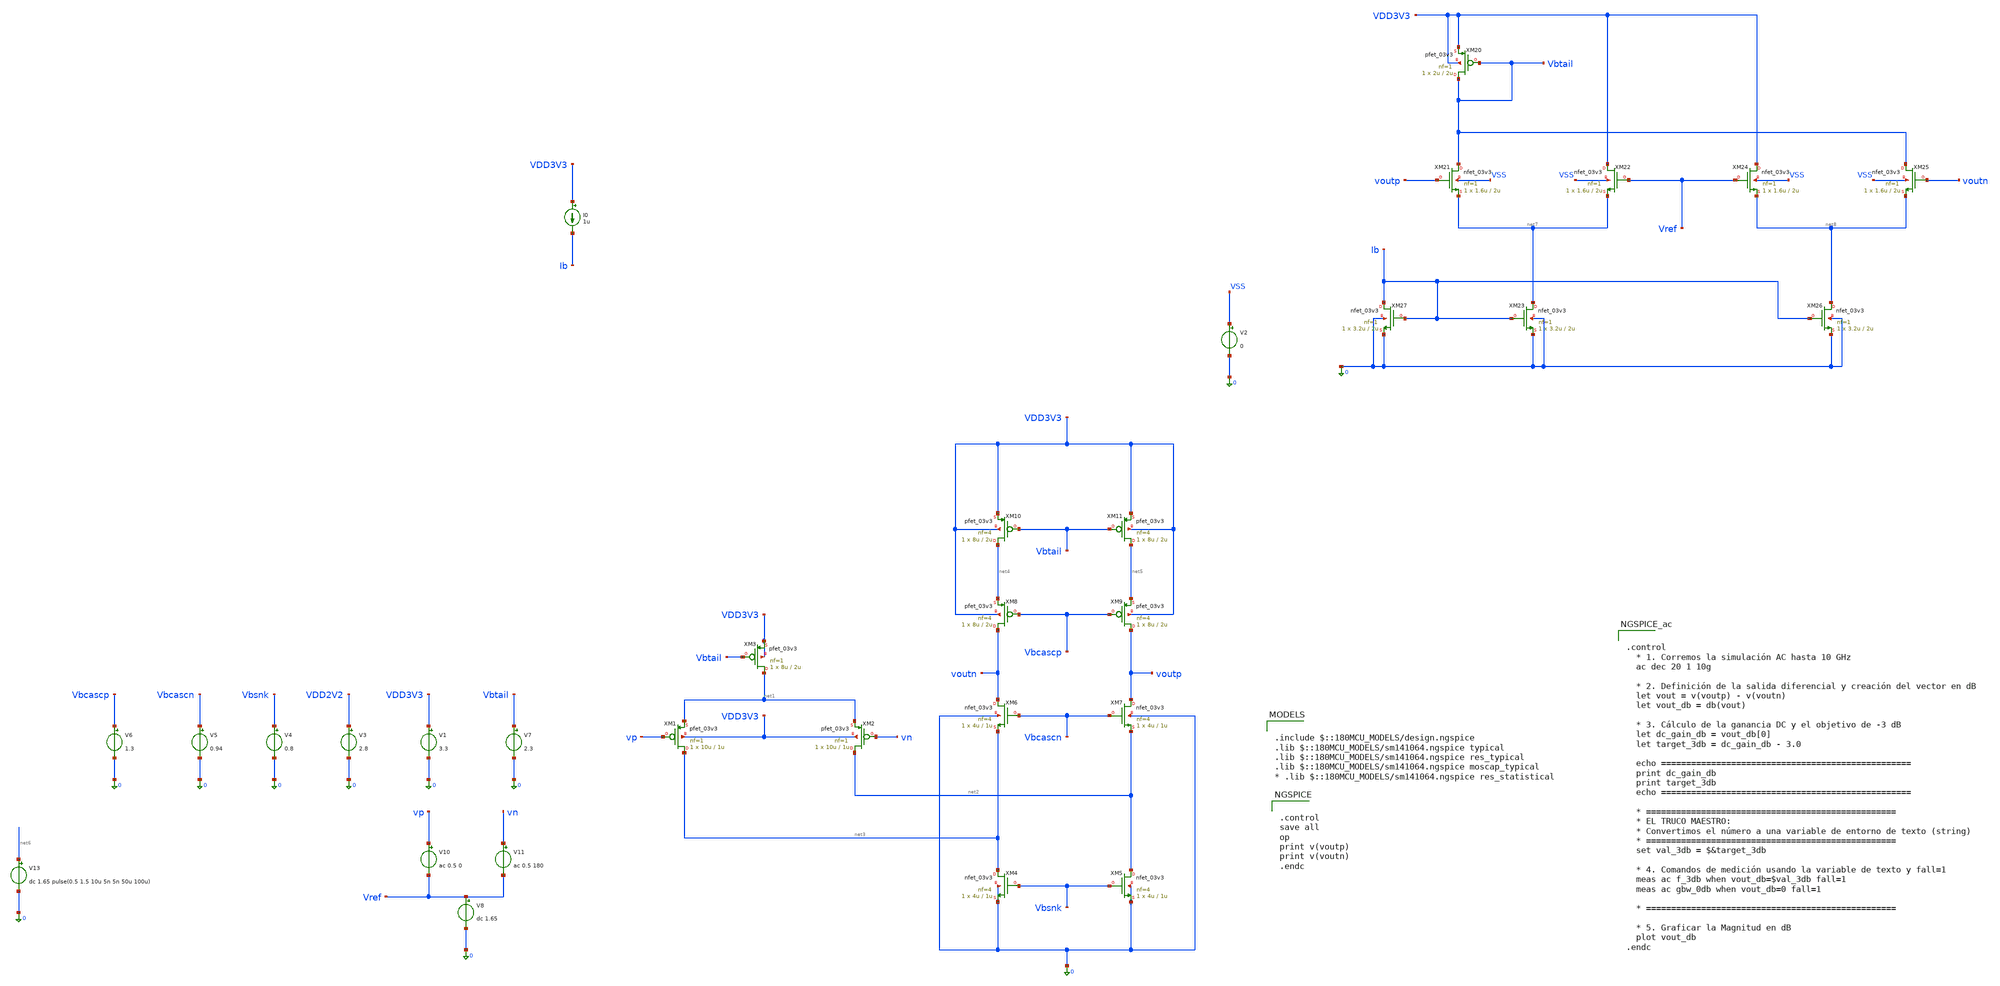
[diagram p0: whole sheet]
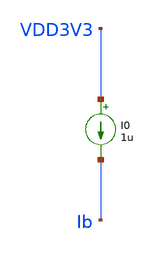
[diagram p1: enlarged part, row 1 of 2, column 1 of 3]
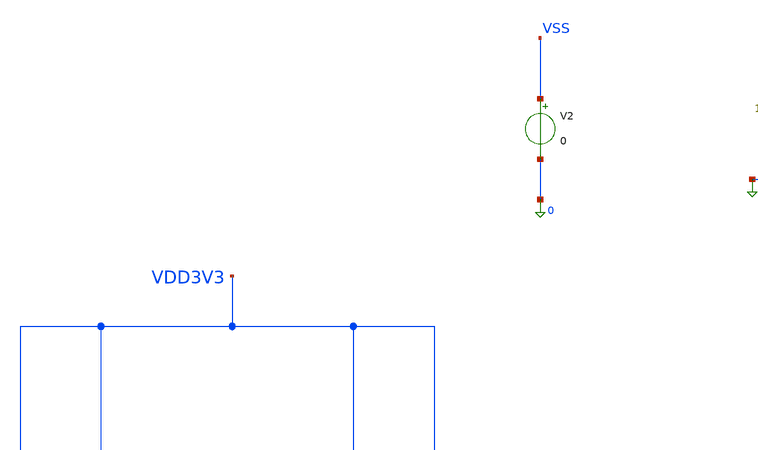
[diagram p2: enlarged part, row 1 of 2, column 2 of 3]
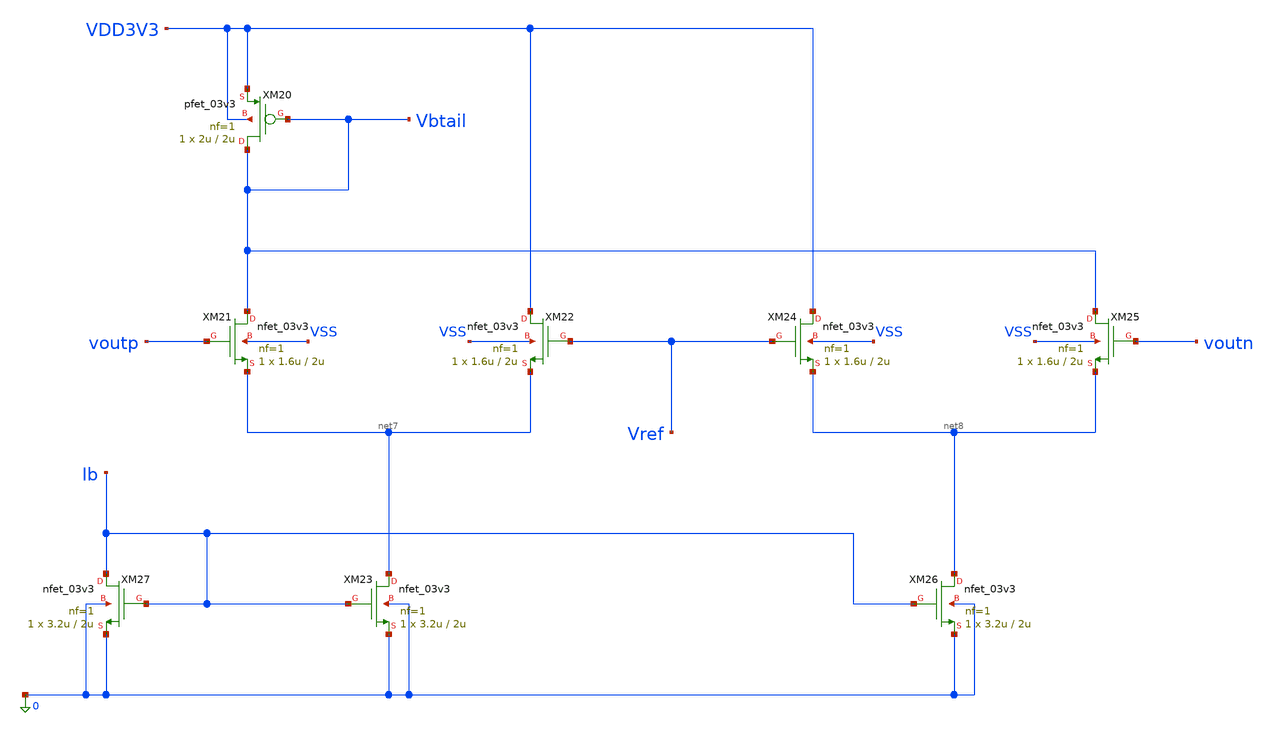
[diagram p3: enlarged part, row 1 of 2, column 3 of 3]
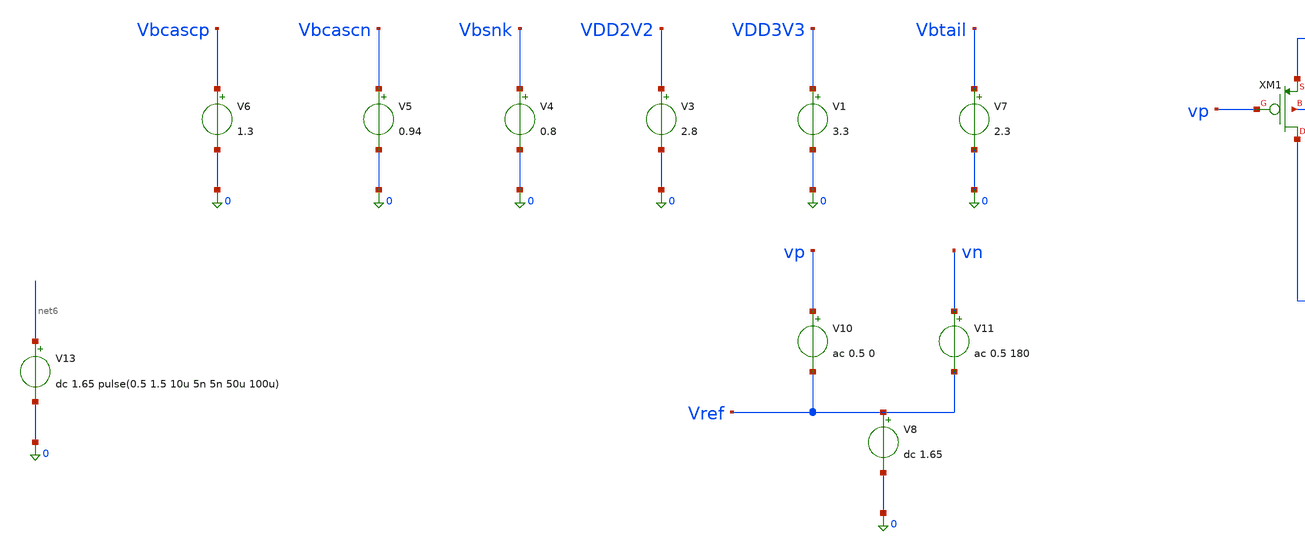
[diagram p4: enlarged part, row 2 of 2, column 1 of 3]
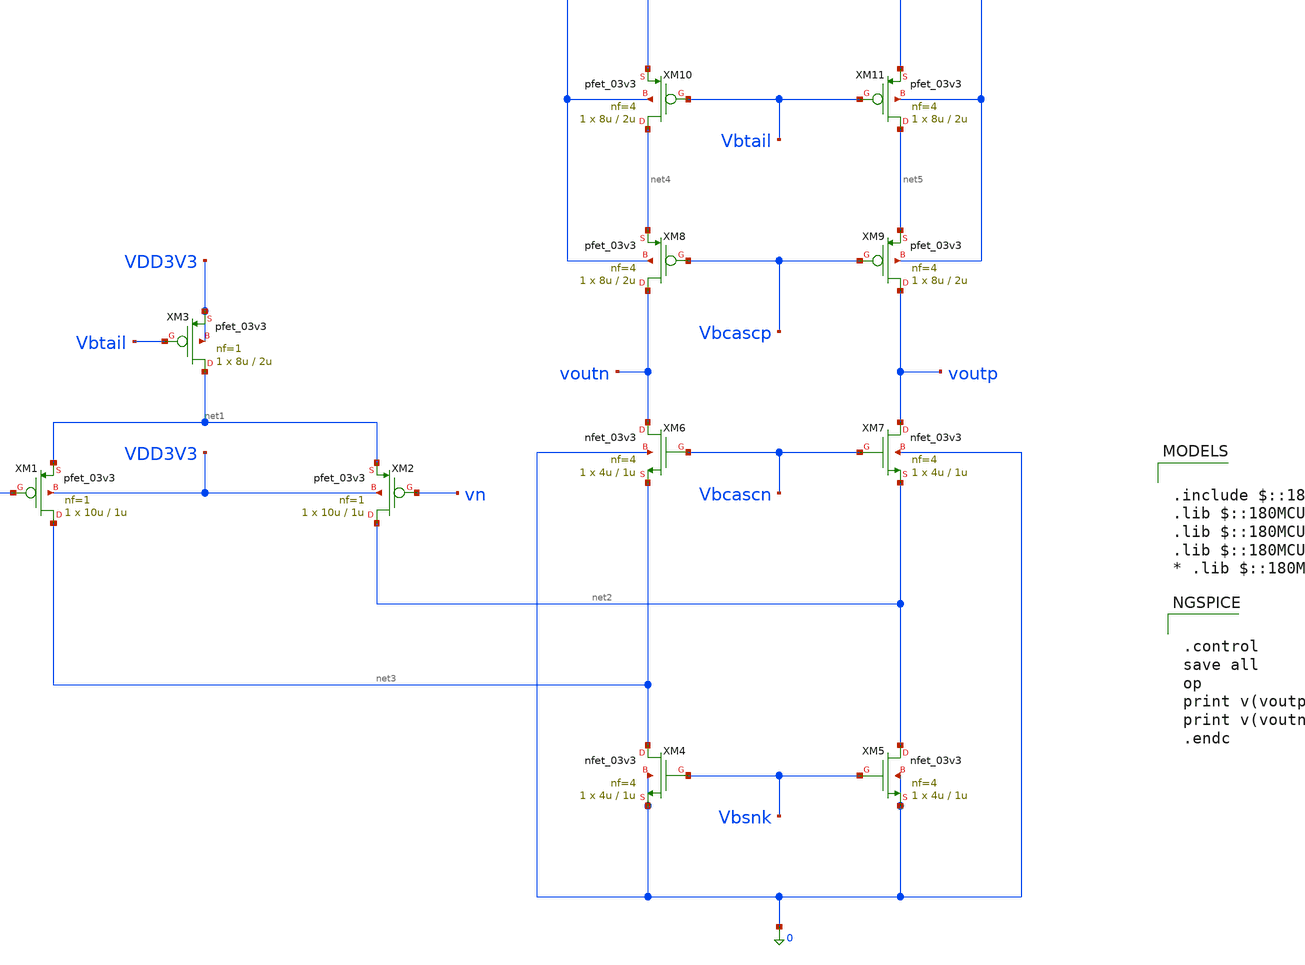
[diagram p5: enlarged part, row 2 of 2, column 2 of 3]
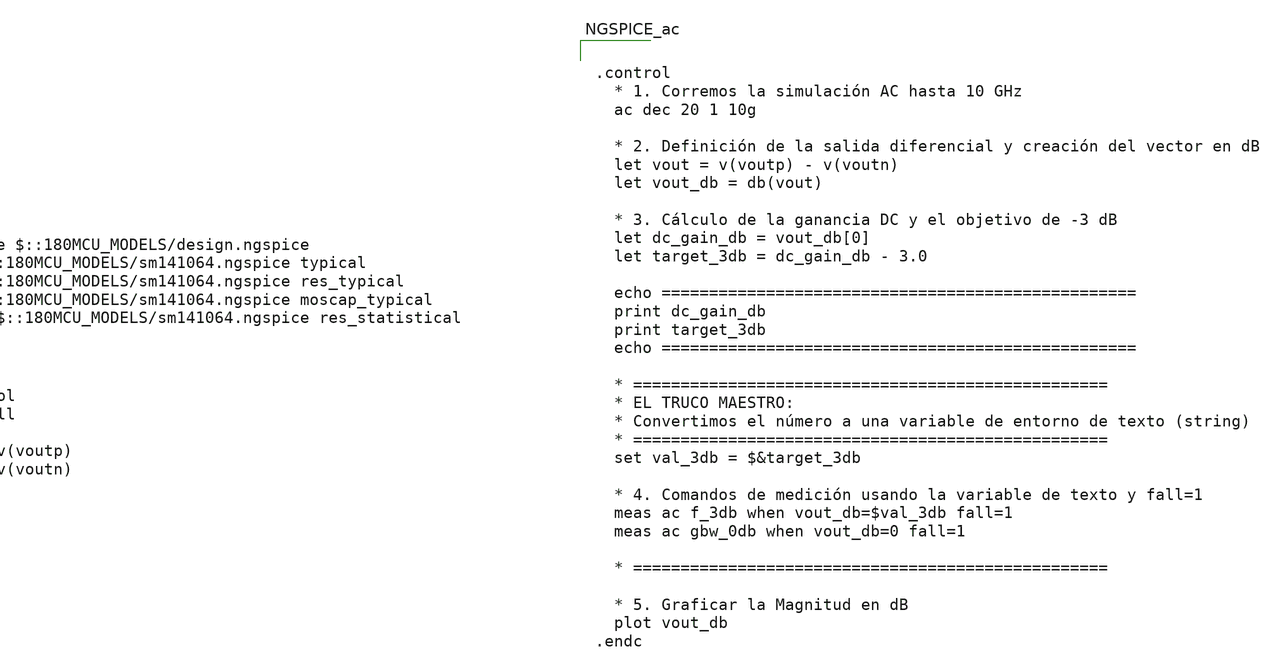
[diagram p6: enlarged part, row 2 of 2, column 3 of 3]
** sch_path: designs/libs/core_pga/folded_cascode/tb_folded_cascode_v2.sch
**.subckt tb_folded_cascode_v2
XM1 net3 vp net1 VDD3V3 pfet_03v3 L=1u W=10u nf=1 ad='int((nf+1)/2) * W/nf * 0.18u' as='int((nf+2)/2) * W/nf * 0.18u'
+ pd='2*int((nf+1)/2) * (W/nf + 0.18u)' ps='2*int((nf+2)/2) * (W/nf + 0.18u)' nrd='0.18u / W' nrs='0.18u / W'
+ sa=0 sb=0 sd=0 m=1
V1 VDD3V3 0 3.3
XM2 net2 vn net1 VDD3V3 pfet_03v3 L=1u W=10u nf=1 ad='int((nf+1)/2) * W/nf * 0.18u' as='int((nf+2)/2) * W/nf * 0.18u'
+ pd='2*int((nf+1)/2) * (W/nf + 0.18u)' ps='2*int((nf+2)/2) * (W/nf + 0.18u)' nrd='0.18u / W' nrs='0.18u / W'
+ sa=0 sb=0 sd=0 m=1
V3 VDD2V2 0 2.8
V4 Vbsnk 0 0.8
V5 Vbcascn 0 0.94
V6 Vbcascp 0 1.3
V8 Vref 0 dc 1.65
V10 vp Vref ac 0.5 0
V11 vn Vref ac 0.5 180
XM6 voutn Vbcascn net3 0 nfet_03v3 L=1u W=4u nf=4 ad='int((nf+1)/2) * W/nf * 0.18u' as='int((nf+2)/2) * W/nf * 0.18u'
+ pd='2*int((nf+1)/2) * (W/nf + 0.18u)' ps='2*int((nf+2)/2) * (W/nf + 0.18u)' nrd='0.18u / W' nrs='0.18u / W'
+ sa=0 sb=0 sd=0 m=1
XM7 voutp Vbcascn net2 0 nfet_03v3 L=1u W=4u nf=4 ad='int((nf+1)/2) * W/nf * 0.18u' as='int((nf+2)/2) * W/nf * 0.18u'
+ pd='2*int((nf+1)/2) * (W/nf + 0.18u)' ps='2*int((nf+2)/2) * (W/nf + 0.18u)' nrd='0.18u / W' nrs='0.18u / W'
+ sa=0 sb=0 sd=0 m=1
XM8 voutn Vbcascp net4 VDD3V3 pfet_03v3 L=2u W=8u nf=4 ad='int((nf+1)/2) * W/nf * 0.18u' as='int((nf+2)/2) * W/nf * 0.18u'
+ pd='2*int((nf+1)/2) * (W/nf + 0.18u)' ps='2*int((nf+2)/2) * (W/nf + 0.18u)' nrd='0.18u / W' nrs='0.18u / W'
+ sa=0 sb=0 sd=0 m=1
XM9 voutp Vbcascp net5 VDD3V3 pfet_03v3 L=2u W=8u nf=4 ad='int((nf+1)/2) * W/nf * 0.18u' as='int((nf+2)/2) * W/nf * 0.18u'
+ pd='2*int((nf+1)/2) * (W/nf + 0.18u)' ps='2*int((nf+2)/2) * (W/nf + 0.18u)' nrd='0.18u / W' nrs='0.18u / W'
+ sa=0 sb=0 sd=0 m=1
V7 Vbtail 0 2.3
XM3 net1 Vbtail VDD3V3 VDD3V3 pfet_03v3 L=2u W=8u nf=1 ad='int((nf+1)/2) * W/nf * 0.18u' as='int((nf+2)/2) * W/nf * 0.18u'
+ pd='2*int((nf+1)/2) * (W/nf + 0.18u)' ps='2*int((nf+2)/2) * (W/nf + 0.18u)' nrd='0.18u / W' nrs='0.18u / W'
+ sa=0 sb=0 sd=0 m=1
XM4 net3 Vbsnk 0 0 nfet_03v3 L=1u W=4u nf=4 ad='int((nf+1)/2) * W/nf * 0.18u' as='int((nf+2)/2) * W/nf * 0.18u'
+ pd='2*int((nf+1)/2) * (W/nf + 0.18u)' ps='2*int((nf+2)/2) * (W/nf + 0.18u)' nrd='0.18u / W' nrs='0.18u / W'
+ sa=0 sb=0 sd=0 m=1
XM5 net2 Vbsnk 0 0 nfet_03v3 L=1u W=4u nf=4 ad='int((nf+1)/2) * W/nf * 0.18u' as='int((nf+2)/2) * W/nf * 0.18u'
+ pd='2*int((nf+1)/2) * (W/nf + 0.18u)' ps='2*int((nf+2)/2) * (W/nf + 0.18u)' nrd='0.18u / W' nrs='0.18u / W'
+ sa=0 sb=0 sd=0 m=1
XM10 net4 Vbtail VDD3V3 VDD3V3 pfet_03v3 L=2u W=8u nf=4 ad='int((nf+1)/2) * W/nf * 0.18u' as='int((nf+2)/2) * W/nf * 0.18u'
+ pd='2*int((nf+1)/2) * (W/nf + 0.18u)' ps='2*int((nf+2)/2) * (W/nf + 0.18u)' nrd='0.18u / W' nrs='0.18u / W'
+ sa=0 sb=0 sd=0 m=1
XM11 net5 Vbtail VDD3V3 VDD3V3 pfet_03v3 L=2u W=8u nf=4 ad='int((nf+1)/2) * W/nf * 0.18u' as='int((nf+2)/2) * W/nf * 0.18u'
+ pd='2*int((nf+1)/2) * (W/nf + 0.18u)' ps='2*int((nf+2)/2) * (W/nf + 0.18u)' nrd='0.18u / W' nrs='0.18u / W'
+ sa=0 sb=0 sd=0 m=1
V13 net6 0 dc 1.65 pulse(0.5 1.5 10u 5n 5n 50u 100u)
I0 VDD3V3 Ib 1u
XM20 Vbtail Vbtail VDD3V3 VDD3V3 pfet_03v3 L=2u W=2u nf=1 ad='int((nf+1)/2) * W/nf * 0.18u' as='int((nf+2)/2) * W/nf * 0.18u'
+ pd='2*int((nf+1)/2) * (W/nf + 0.18u)' ps='2*int((nf+2)/2) * (W/nf + 0.18u)' nrd='0.18u / W' nrs='0.18u / W'
+ sa=0 sb=0 sd=0 m=1
XM21 Vbtail voutp net7 VSS nfet_03v3 L=2u W=1.6u nf=1 ad='int((nf+1)/2) * W/nf * 0.18u' as='int((nf+2)/2) * W/nf * 0.18u'
+ pd='2*int((nf+1)/2) * (W/nf + 0.18u)' ps='2*int((nf+2)/2) * (W/nf + 0.18u)' nrd='0.18u / W' nrs='0.18u / W'
+ sa=0 sb=0 sd=0 m=1
XM22 VDD3V3 Vref net7 VSS nfet_03v3 L=2u W=1.6u nf=1 ad='int((nf+1)/2) * W/nf * 0.18u' as='int((nf+2)/2) * W/nf * 0.18u'
+ pd='2*int((nf+1)/2) * (W/nf + 0.18u)' ps='2*int((nf+2)/2) * (W/nf + 0.18u)' nrd='0.18u / W' nrs='0.18u / W'
+ sa=0 sb=0 sd=0 m=1
XM23 net7 Ib 0 0 nfet_03v3 L=2u W=3.2u nf=1 ad='int((nf+1)/2) * W/nf * 0.18u' as='int((nf+2)/2) * W/nf * 0.18u'
+ pd='2*int((nf+1)/2) * (W/nf + 0.18u)' ps='2*int((nf+2)/2) * (W/nf + 0.18u)' nrd='0.18u / W' nrs='0.18u / W'
+ sa=0 sb=0 sd=0 m=1
XM24 VDD3V3 Vref net8 VSS nfet_03v3 L=2u W=1.6u nf=1 ad='int((nf+1)/2) * W/nf * 0.18u' as='int((nf+2)/2) * W/nf * 0.18u'
+ pd='2*int((nf+1)/2) * (W/nf + 0.18u)' ps='2*int((nf+2)/2) * (W/nf + 0.18u)' nrd='0.18u / W' nrs='0.18u / W'
+ sa=0 sb=0 sd=0 m=1
XM25 Vbtail voutn net8 VSS nfet_03v3 L=2u W=1.6u nf=1 ad='int((nf+1)/2) * W/nf * 0.18u' as='int((nf+2)/2) * W/nf * 0.18u'
+ pd='2*int((nf+1)/2) * (W/nf + 0.18u)' ps='2*int((nf+2)/2) * (W/nf + 0.18u)' nrd='0.18u / W' nrs='0.18u / W'
+ sa=0 sb=0 sd=0 m=1
XM26 net8 Ib 0 0 nfet_03v3 L=2u W=3.2u nf=1 ad='int((nf+1)/2) * W/nf * 0.18u' as='int((nf+2)/2) * W/nf * 0.18u'
+ pd='2*int((nf+1)/2) * (W/nf + 0.18u)' ps='2*int((nf+2)/2) * (W/nf + 0.18u)' nrd='0.18u / W' nrs='0.18u / W'
+ sa=0 sb=0 sd=0 m=1
XM27 Ib Ib 0 0 nfet_03v3 L=2u W=3.2u nf=1 ad='int((nf+1)/2) * W/nf * 0.18u' as='int((nf+2)/2) * W/nf * 0.18u'
+ pd='2*int((nf+1)/2) * (W/nf + 0.18u)' ps='2*int((nf+2)/2) * (W/nf + 0.18u)' nrd='0.18u / W' nrs='0.18u / W'
+ sa=0 sb=0 sd=0 m=1
V2 VSS 0 0
**** begin user architecture code

.include $::180MCU_MODELS/design.ngspice
.lib $::180MCU_MODELS/sm141064.ngspice typical
.lib $::180MCU_MODELS/sm141064.ngspice res_typical
.lib $::180MCU_MODELS/sm141064.ngspice moscap_typical
* .lib $::180MCU_MODELS/sm141064.ngspice res_statistical



.control
save all
op
print v(voutp)
print v(voutn)
.endc




.control
  * 1. Corremos la simulación AC hasta 10 GHz
  ac dec 20 1 10g

  * 2. Definición de la salida diferencial y creación del vector en dB
  let vout = v(voutp) - v(voutn)
  let vout_db = db(vout)

  * 3. Cálculo de la ganancia DC y el objetivo de -3 dB
  let dc_gain_db = vout_db[0]
  let target_3db = dc_gain_db - 3.0

  echo ==================================================
  print dc_gain_db
  print target_3db
  echo ==================================================

  * ==================================================
  * EL TRUCO MAESTRO:
  * Convertimos el número a una variable de entorno de texto (string)
  * ==================================================
  set val_3db = $&target_3db

  * 4. Comandos de medición usando la variable de texto y fall=1
  meas ac f_3db when vout_db=$val_3db fall=1
  meas ac gbw_0db when vout_db=0 fall=1

  * ==================================================

  * 5. Graficar la Magnitud en dB
  plot vout_db
.endc


**** end user architecture code
**.ends
.end
